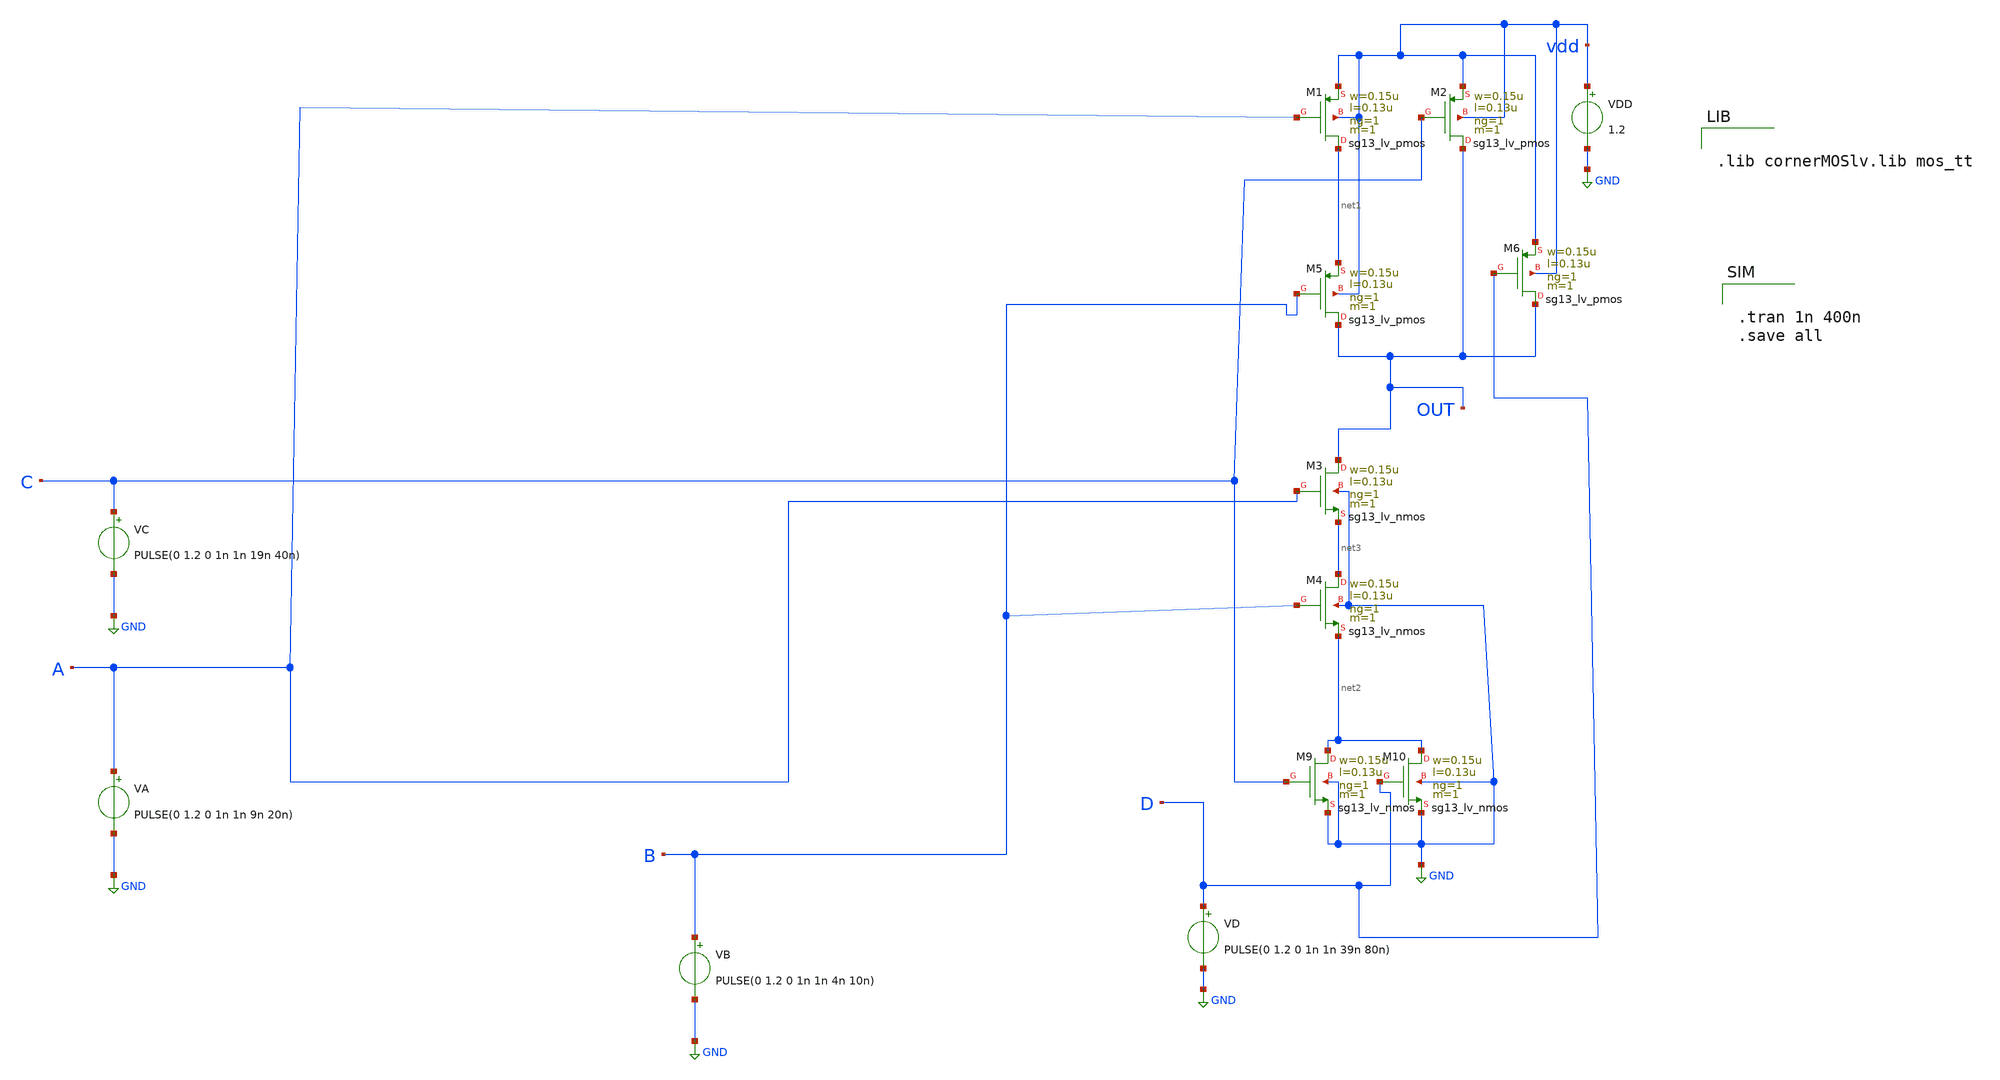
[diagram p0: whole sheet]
** sch_path: aoi211.sch
**.subckt aoi211
XM1 net1 A vdd vdd sg13_lv_pmos w=0.15u l=0.13u ng=1 m=1 mm_ok=1
XM2 OUT C vdd vdd sg13_lv_pmos w=0.15u l=0.13u ng=1 m=1 mm_ok=1
XM3 OUT A net3 GND sg13_lv_nmos w=0.15u l=0.13u ng=1 m=1 mm_ok=1
XM4 net3 B net2 GND sg13_lv_nmos w=0.15u l=0.13u ng=1 m=1 mm_ok=1
VDD vdd GND 1.2
VA A GND PULSE(0 1.2 0 1n 1n 9n 20n)
VB B GND PULSE(0 1.2 0 1n 1n 4n 10n)
XM5 OUT B net1 vdd sg13_lv_pmos w=0.15u l=0.13u ng=1 m=1 mm_ok=1
VC C GND PULSE(0 1.2 0 1n 1n 19n 40n)
VD D GND PULSE(0 1.2 0 1n 1n 39n 80n)
XM6 OUT D vdd vdd sg13_lv_pmos w=0.15u l=0.13u ng=1 m=1 mm_ok=1
XM9 net2 C GND GND sg13_lv_nmos w=0.15u l=0.13u ng=1 m=1 mm_ok=1
XM10 net2 D GND GND sg13_lv_nmos w=0.15u l=0.13u ng=1 m=1 mm_ok=1
**** begin user architecture code


.lib cornerMOSlv.lib mos_tt



.tran 1n 400n
.save all


**** end user architecture code
**.ends
.GLOBAL GND
.end
